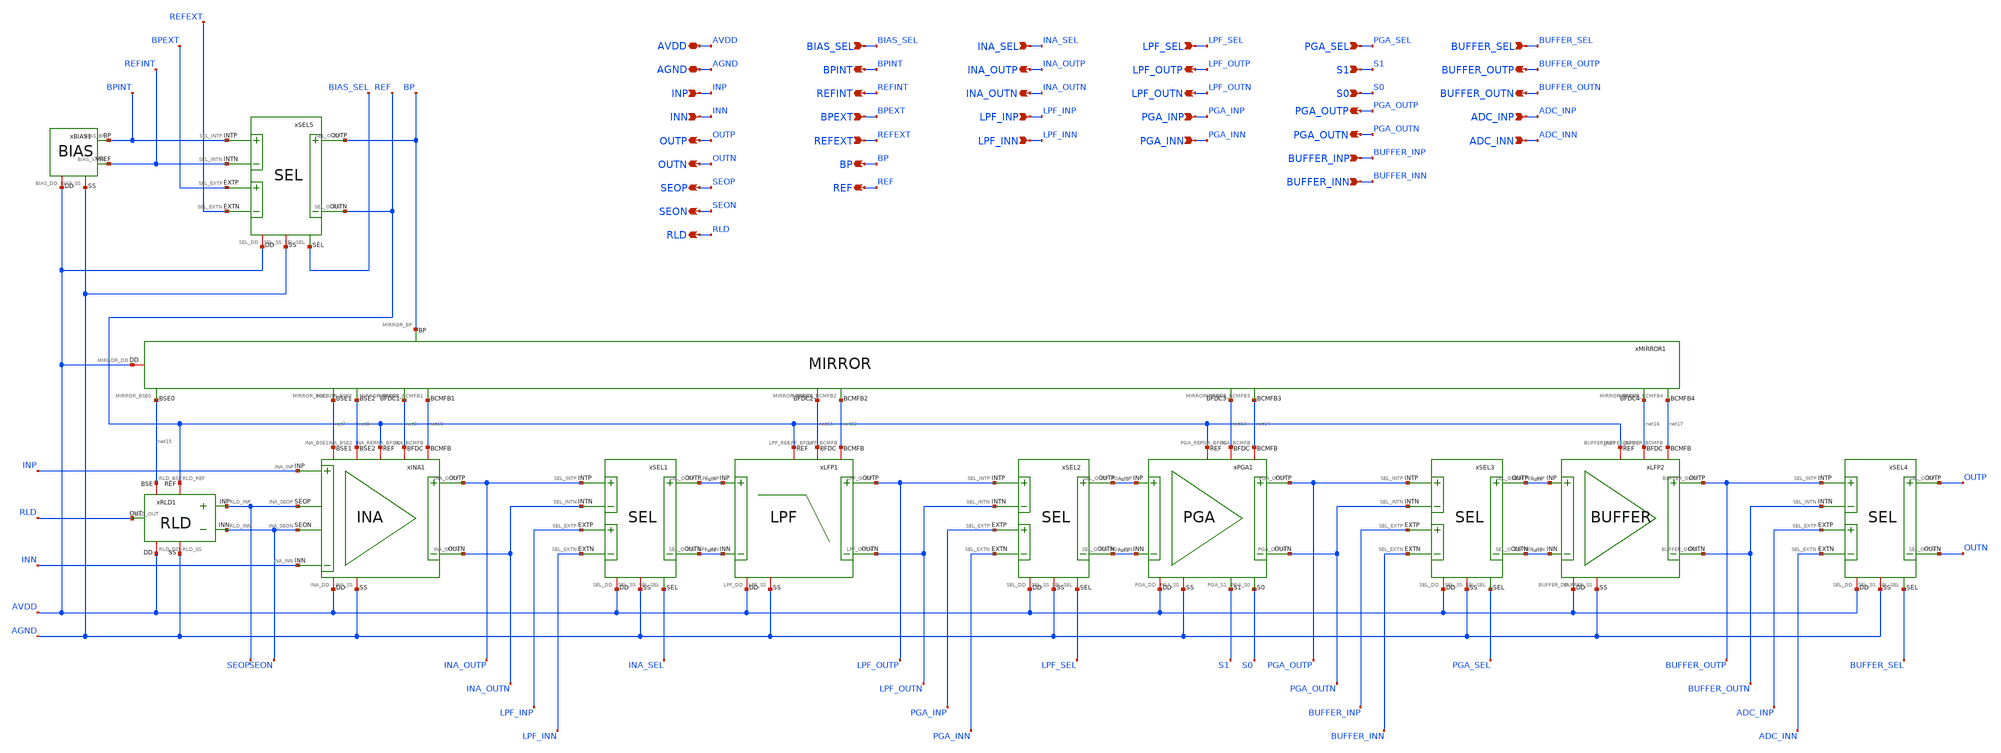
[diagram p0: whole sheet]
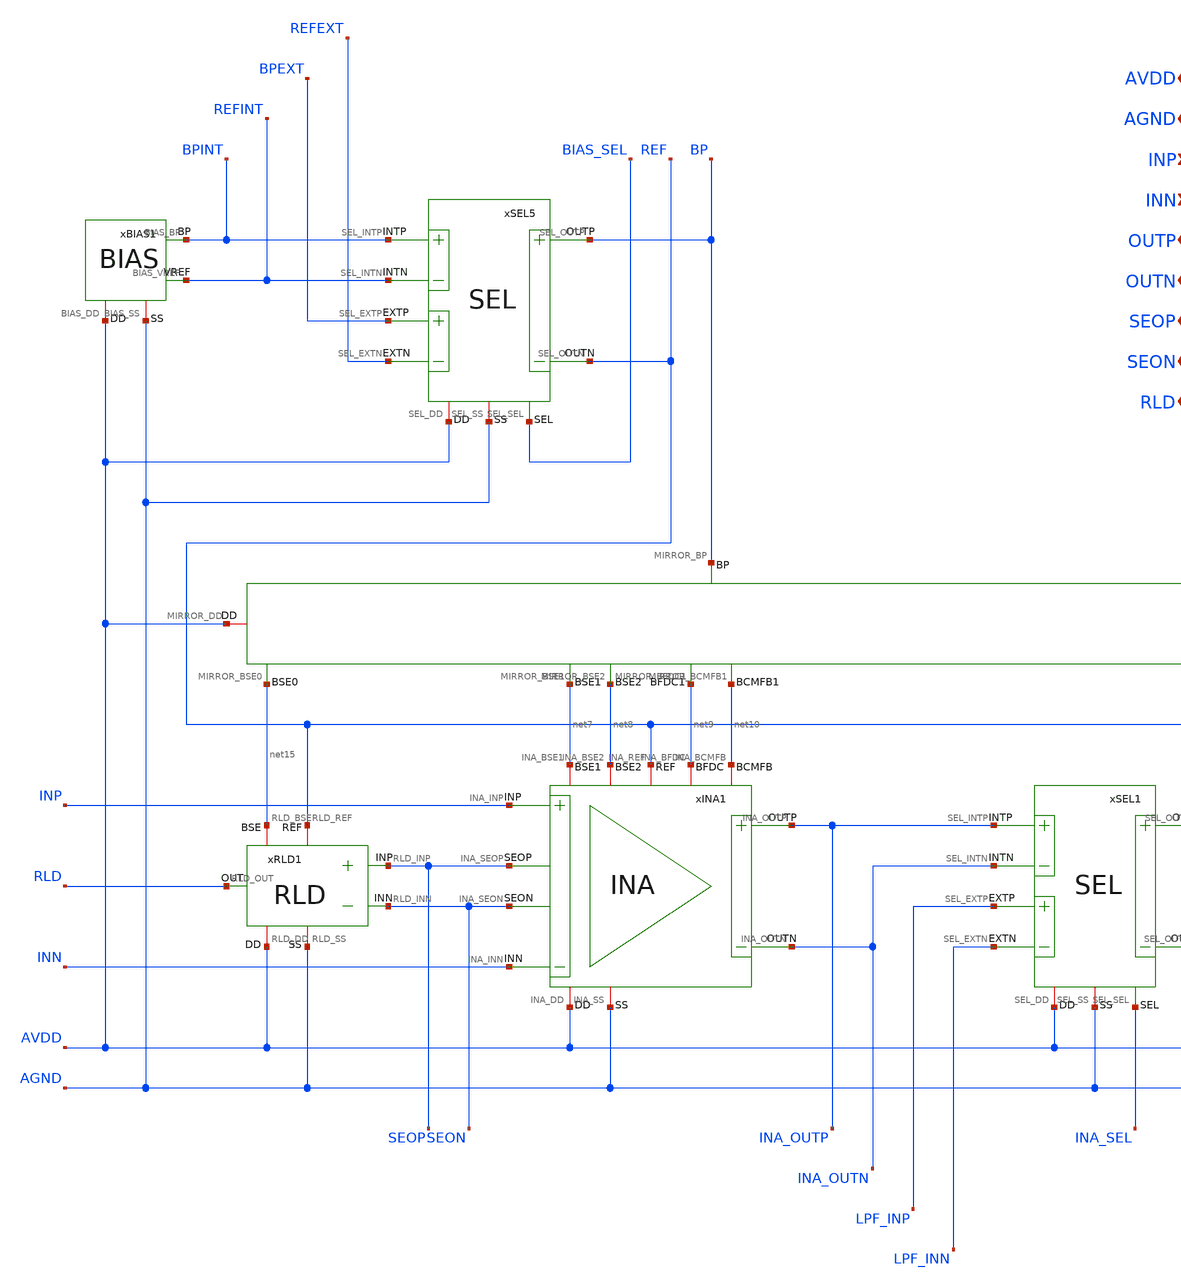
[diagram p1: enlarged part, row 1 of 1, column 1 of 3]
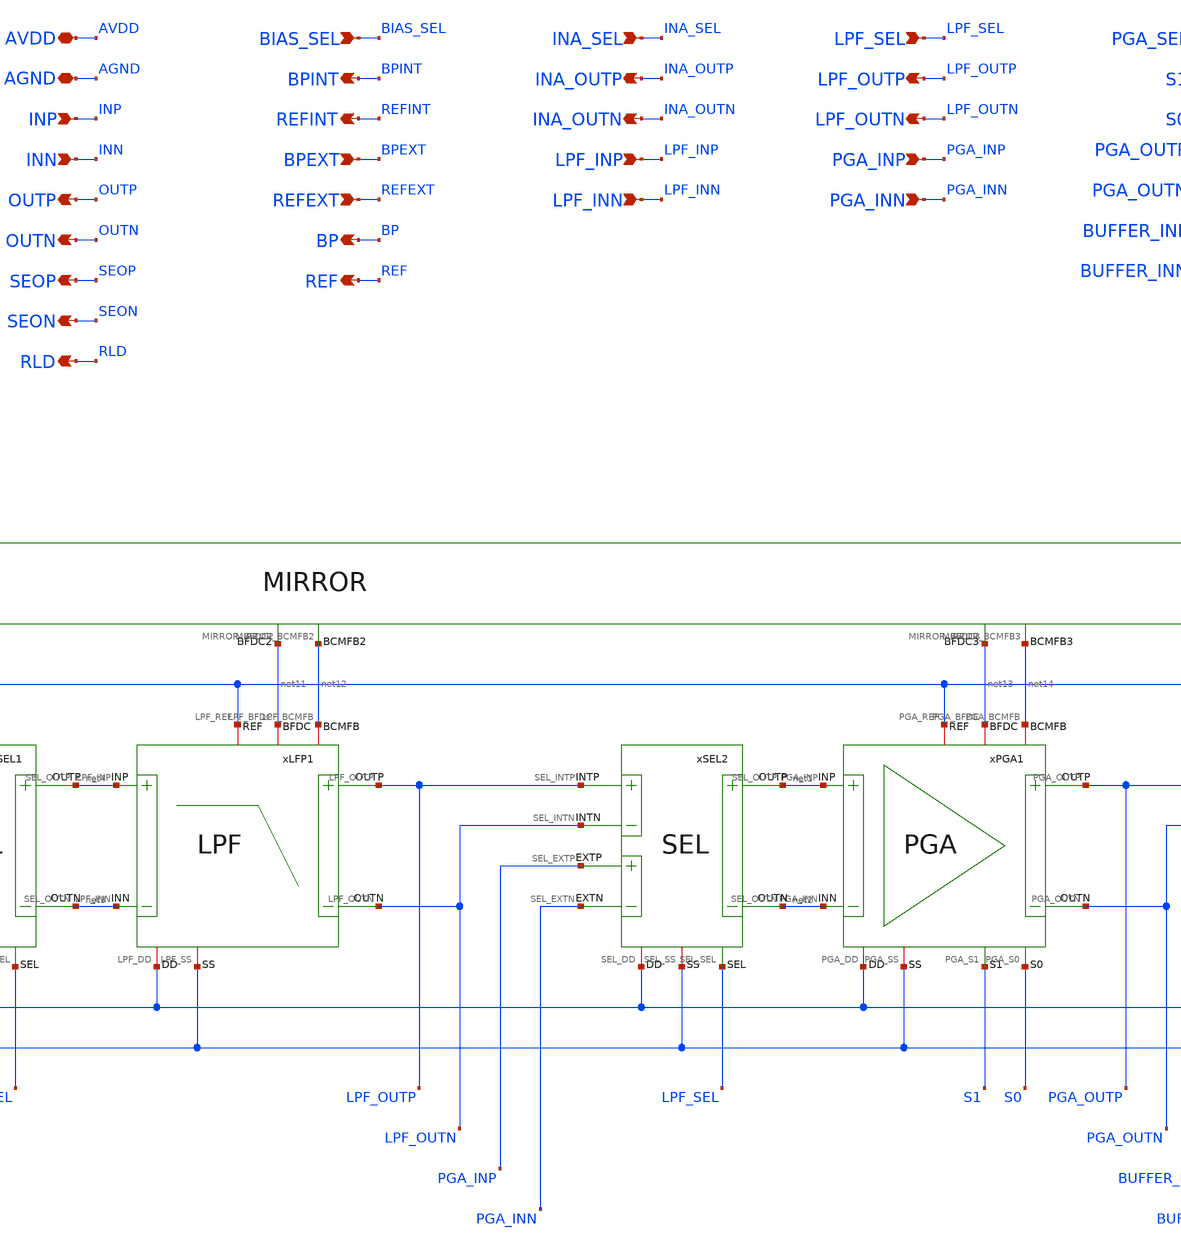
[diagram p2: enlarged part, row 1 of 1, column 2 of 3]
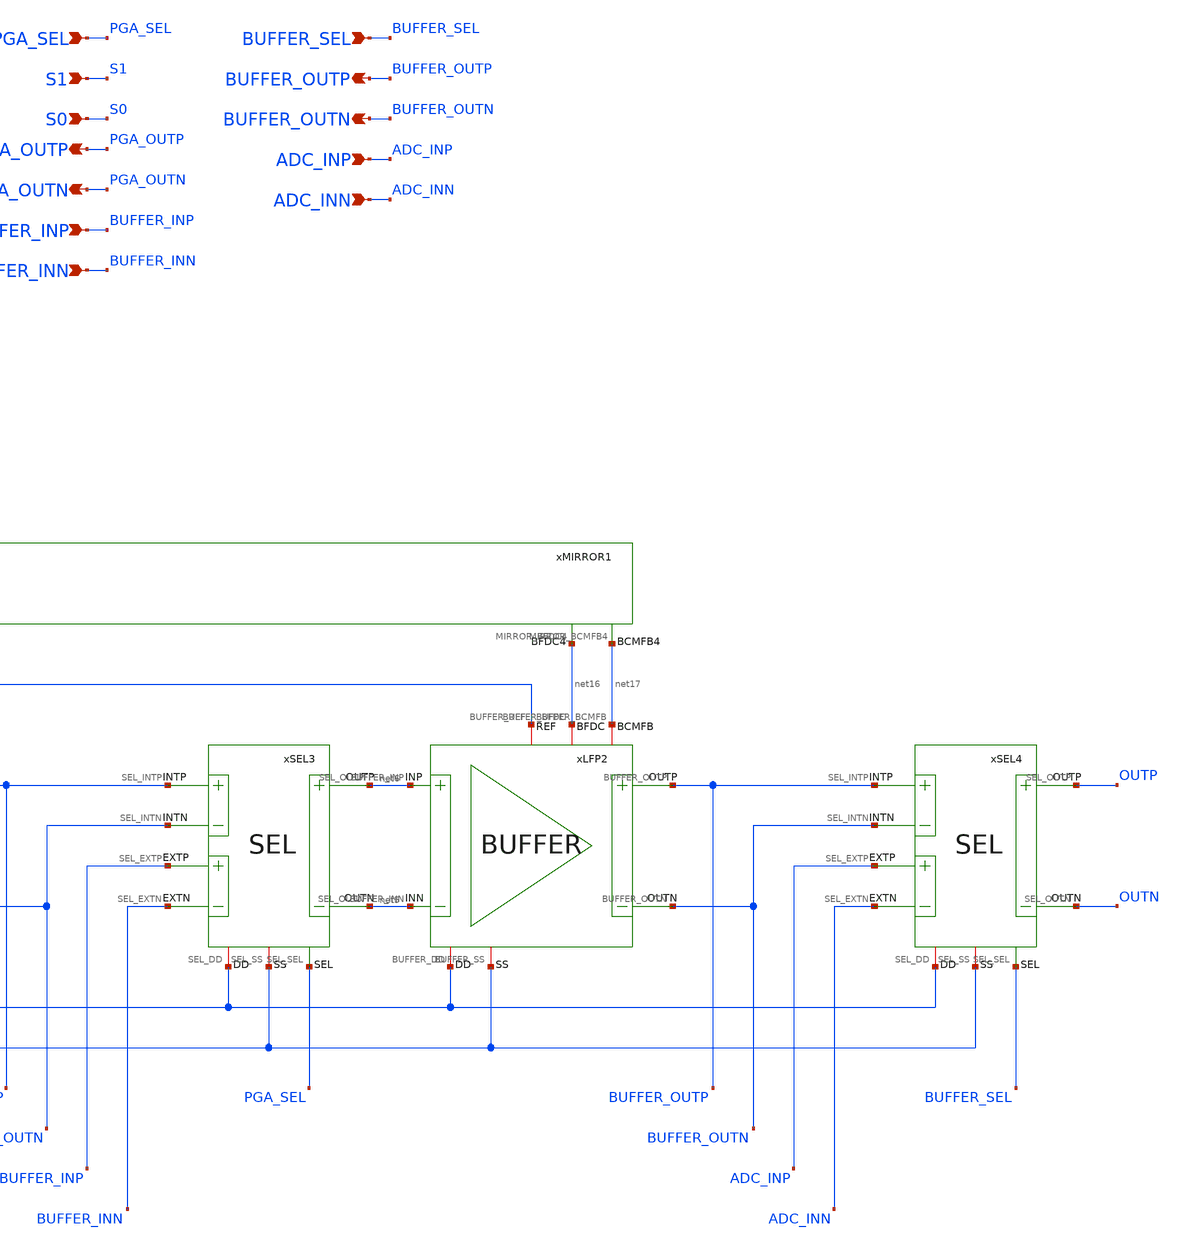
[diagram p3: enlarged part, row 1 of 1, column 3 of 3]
** sch_path: Design_Files/IC Design/Schematic/AFE/AFE.sch
**.subckt AFE INA_OUTP INA_OUTN LPF_INP LPF_INN LPF_OUTP LPF_OUTN PGA_INP PGA_INN PGA_OUTP PGA_OUTN
*+ BUFFER_INP BUFFER_INN BUFFER_OUTP BUFFER_OUTN ADC_INP ADC_INN AVDD AGND SEOP SEON RLD INP INN BPINT REFINT
*+ BPEXT REFEXT BIAS_SEL BP REF INA_SEL LPF_SEL PGA_SEL S1 S0 BUFFER_SEL OUTP OUTN
*.opin INA_OUTP
*.opin INA_OUTN
*.ipin LPF_INP
*.ipin LPF_INN
*.opin LPF_OUTP
*.opin LPF_OUTN
*.ipin PGA_INP
*.ipin PGA_INN
*.opin PGA_OUTP
*.opin PGA_OUTN
*.ipin BUFFER_INP
*.ipin BUFFER_INN
*.opin BUFFER_OUTP
*.opin BUFFER_OUTN
*.ipin ADC_INP
*.ipin ADC_INN
*.iopin AVDD
*.iopin AGND
*.opin SEOP
*.opin SEON
*.opin RLD
*.ipin INP
*.ipin INN
*.opin BPINT
*.opin REFINT
*.ipin BPEXT
*.ipin REFEXT
*.ipin BIAS_SEL
*.opin BP
*.opin REF
*.ipin INA_SEL
*.ipin LPF_SEL
*.ipin PGA_SEL
*.ipin S1
*.ipin S0
*.ipin BUFFER_SEL
*.opin OUTP
*.opin OUTN
xLFP1 AVDD AGND net4 net3 LPF_OUTN net11 LPF_OUTP net12 REF LPF
xPGA1 AVDD AGND net1 net2 PGA_OUTN net13 PGA_OUTP net14 REF S1 S0 PGA
xSEL1 AVDD AGND INA_OUTP INA_OUTN net3 net4 LPF_INP LPF_INN INA_SEL SEL
xINA1 AVDD AGND INP INN INA_OUTN net9 INA_OUTP net10 REF SEON SEOP net7 net8 INA
xSEL2 AVDD AGND LPF_OUTP LPF_OUTN net2 net1 PGA_INP PGA_INN LPF_SEL SEL
xSEL3 AVDD AGND PGA_OUTP PGA_OUTN net5 net6 BUFFER_INP BUFFER_INN PGA_SEL SEL
xSEL4 AVDD AGND BUFFER_OUTP BUFFER_OUTN OUTN OUTP ADC_INP ADC_INN BUFFER_SEL SEL
xLFP2 AVDD AGND net6 net5 BUFFER_OUTN net16 BUFFER_OUTP net17 REF BUFFER
xRLD1 AVDD AGND SEOP SEON RLD REF net15 RLD
xBIAS1 AVDD AGND BPINT REFINT BIAS
xSEL5 AVDD AGND BPINT REFINT REF BP BPEXT REFEXT BIAS_SEL SEL
xMIRROR1 AVDD BP net15 net7 net8 net9 net11 net13 net16 net10 net12 net14 net17 MIRROR
**.ends
.end
